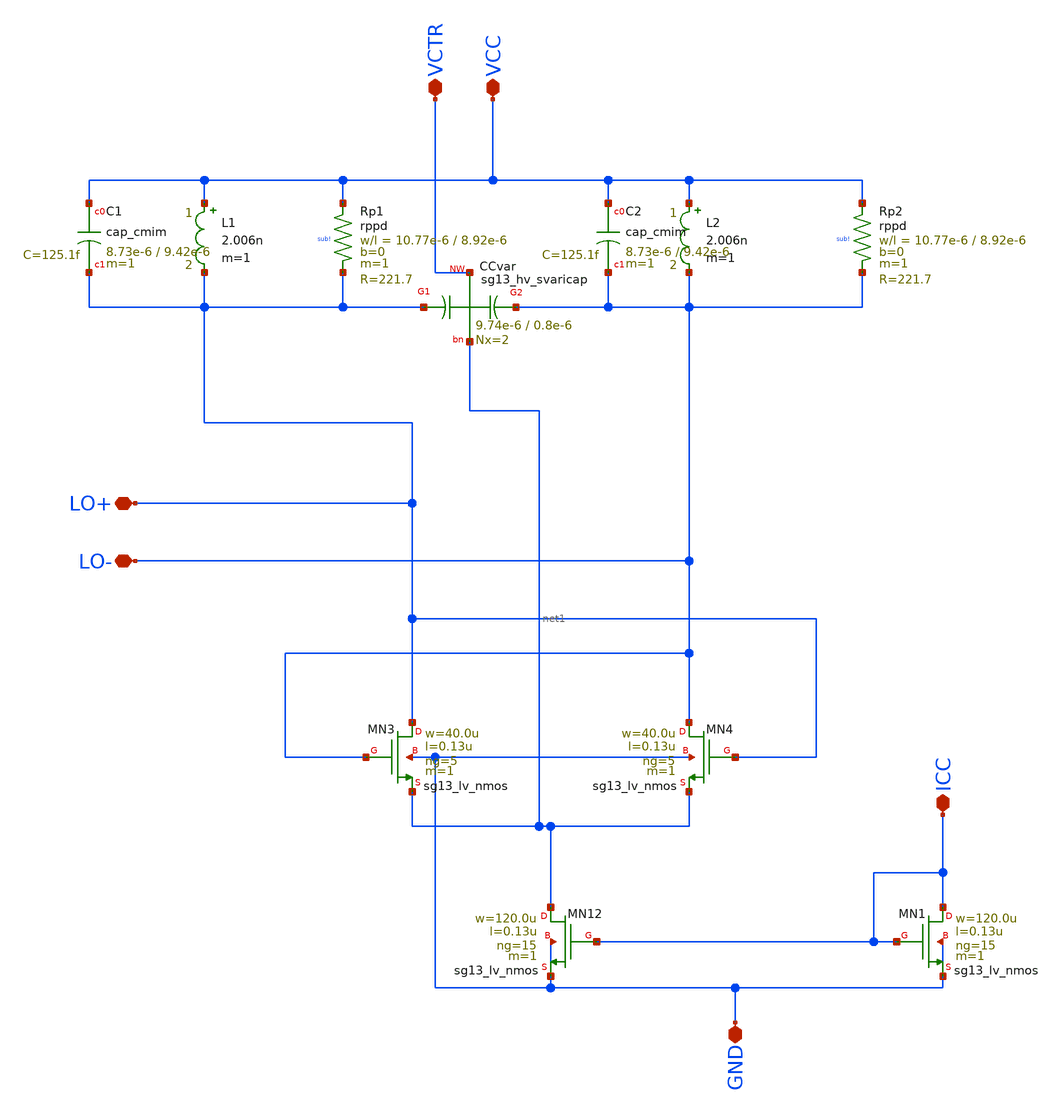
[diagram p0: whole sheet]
** sch_path: Schematic/LC_VCO.sch
**.subckt LC_VCO LO- LO+ VCC ICC GND VCTR
*.iopin LO-
*.iopin LO+
*.iopin VCC
*.iopin ICC
*.iopin GND
*.iopin VCTR
XMN3 LO+ LO- net1 GND sg13_lv_nmos w=40.0u l=0.13u ng=5 m=1 mm_ok=1
XMN4 LO- LO+ net1 GND sg13_lv_nmos w=40.0u l=0.13u ng=5 m=1 mm_ok=1
XMN1 ICC ICC GND GND sg13_lv_nmos w=120.0u l=0.13u ng=15 m=1 mm_ok=1
XMN12 net1 ICC GND GND sg13_lv_nmos w=120.0u l=0.13u ng=15 m=1 mm_ok=1
XC1 VCC LO+ cap_cmim w=8.73e-6 l=9.42e-6 m=1 mm_ok=1
XRp1 VCC LO+ sub! rppd w=10.77e-6 l=8.92e-6 m=1 b=0 mm_ok=1
XC2 VCC LO- cap_cmim w=8.73e-6 l=9.42e-6 m=1 mm_ok=1
XRp2 VCC LO- sub! rppd w=10.77e-6 l=8.92e-6 m=1 b=0 mm_ok=1
L1 VCC LO+ 2.006n m=1
L2 VCC LO- 2.006n m=1
XCvar LO+ VCTR LO- net1 sg13_hv_svaricap w=9.74e-6 l=0.8e-6 Nx=2
**.ends
.end
